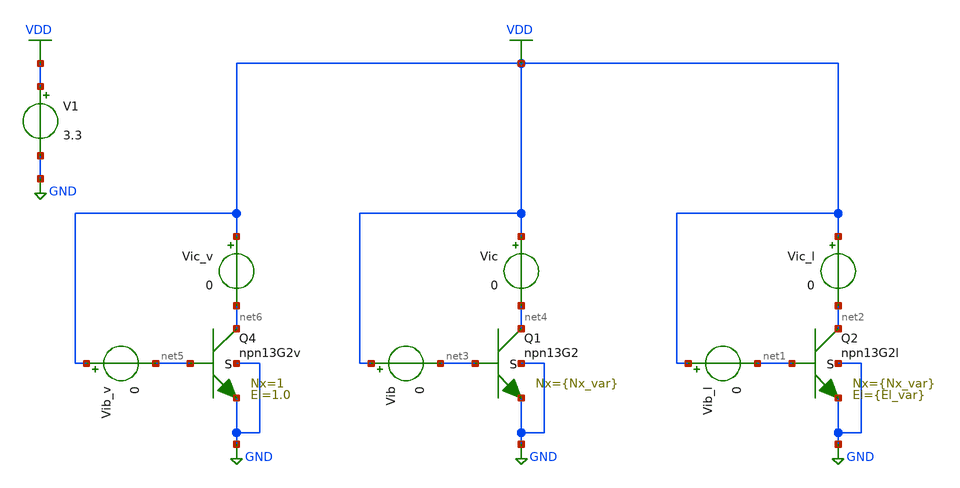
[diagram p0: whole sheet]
** sch_path: sim_backup/simulations/try.sch
**.subckt try
XQ2 net2 net1 GND GND npn13G2l Nx={Nx_var} El={El_var} mm_ok=1
V1 VDD GND 3.3
Vib_l VDD net1 0
Vic_l VDD net2 0
xQ1 net4 net3 GND GND npn13G2 Nx={Nx_var} mm_ok=1
Vib VDD net3 0
Vic VDD net4 0
Vib_v VDD net5 0
Vic_v VDD net6 0
XQ4 net6 net5 GND GND npn13G2v Nx=1 El=1.0 mm_ok=1
**** begin user architecture code


.lib /foss/pdks/ihp-sg13g2/libs.tech/ngspice/models/cornerHBT.lib hbt_typ

.param El_var = 1 temper = 27 Nx_var = 1
.temp {temper}
.op
.control
;control of changing params Nx (number of emitter in a row)
set plotib = ' ';
set plotib_l = ' ';
set plotib_v = ' ';
set plotic = ' ';
set plotic_l = ' ';
set plotic_v = ' ';
set plotbeta = ' ';
set plotbeta_v = ' ';
set plotbeta_l = ' ';
let Nx_1 = 1

repeat 10;
	alterparam Nx_var = $&Nx_1
	reset
	dc V1 0.1 1.6 0.05
	if Nx_var < 5
		set plotib_l = ( $plotib_l ({$curplot}.I(Vib_l)) );
		set plotic_l = ( $plotic_l ({$curplot}.I(Vic_l)) );
		set plotbeta_l = ( $plotbeta_l {$curplot}.I(vic_l)/{$curplot}.I(vib_l) );
	if Nx_var < 9
		set plotib_v = ( $plotib_v ({$curplot}.I(Vib_v)) );
		set plotic_v = ( $plotic_v ({$curplot}.I(Vic_v)) );
		set plotbeta_v = ( $plotbeta_v {$curplot}.I(vic_v)/{$curplot}.I(vib_v) );
	set plotib =   ( $plotib ({$curplot}.I(Vib)) );
	set plotic =   ( $plotic   ({$curplot}.I(Vic)) );
	set plotbeta =   ( $plotbeta {$curplot}.I(vic)/{$curplot}.I(vib) );
	let Nx_1 = Nx_1 + 1
end;

plot loglog $plotib $plotib_l $plotib_v;
plot loglog $plotic $plotic_l $plotic_v;
plot loglog $plotbeta $plotbeta_l $plotbeta_v;
plot loglog ($plotbeta) vs ($plotic);
;set wr_singlescale;
;set wr_vecnames;
;wrdata gummel_npn13g2_Nx.txt $plotib $plotic $plotbeta;
;wrdata gummel_npn13g2l_Nx.txt $plotib_l $plotic_l $plotbeta_l;
;wrdata gummel_npn13g2v_Nx.txt $plotib_v $plotic_v $plotbeta_v;

.endc

.save all


**** end user architecture code
**.ends
.GLOBAL GND
.GLOBAL VDD
.end
